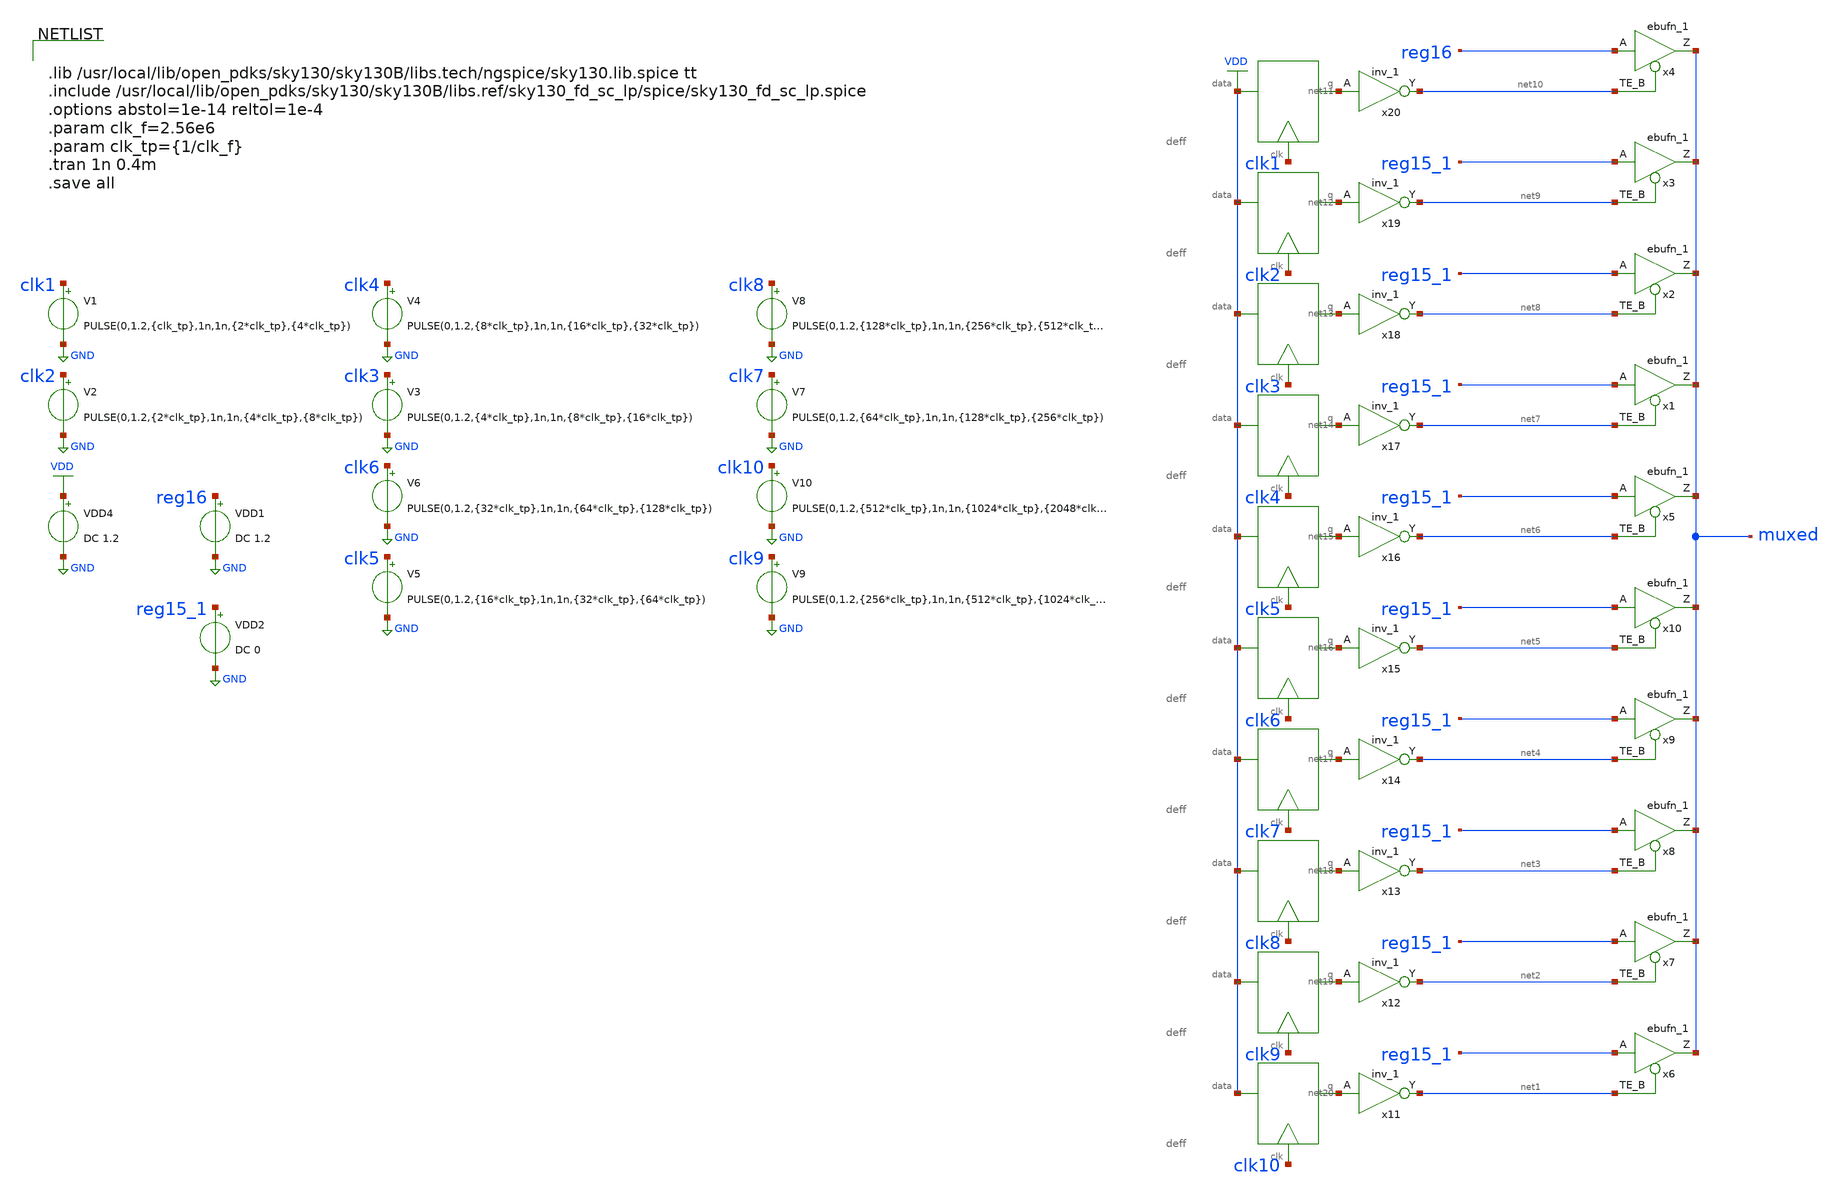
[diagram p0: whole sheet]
** sch_path: xschem/tryandtest/grayselection.sch
**.subckt grayselection
V1 clk1 GND PULSE(0,1.2,{clk_tp},1n,1n,{2*clk_tp},{4*clk_tp})
VDD4 VDD GND DC 1.2
V2 clk2 GND PULSE(0,1.2,{2*clk_tp},1n,1n,{4*clk_tp},{8*clk_tp})
V3 clk3 GND PULSE(0,1.2,{4*clk_tp},1n,1n,{8*clk_tp},{16*clk_tp})
V4 clk4 GND PULSE(0,1.2,{8*clk_tp},1n,1n,{16*clk_tp},{32*clk_tp})
V5 clk5 GND PULSE(0,1.2,{16*clk_tp},1n,1n,{32*clk_tp},{64*clk_tp})
V6 clk6 GND PULSE(0,1.2,{32*clk_tp},1n,1n,{64*clk_tp},{128*clk_tp})
V7 clk7 GND PULSE(0,1.2,{64*clk_tp},1n,1n,{128*clk_tp},{256*clk_tp})
V8 clk8 GND PULSE(0,1.2,{128*clk_tp},1n,1n,{256*clk_tp},{512*clk_tp})
V9 clk9 GND PULSE(0,1.2,{256*clk_tp},1n,1n,{512*clk_tp},{1024*clk_tp})
V10 clk10 GND PULSE(0,1.2,{512*clk_tp},1n,1n,{1024*clk_tp},{2048*clk_tp})
VDD1 reg16 GND DC 1.2
VDD2 reg15_1 GND DC 0
X1 VDD clk1 net11 deff
X1 VDD clk2 net12 deff
X1 VDD clk3 net13 deff
X1 VDD clk4 net14 deff
X1 VDD clk5 net15 deff
x5 reg15_1 net6 GND GND VDD VDD muxed sky130_fd_sc_lp__ebufn_1
X1 VDD clk6 net16 deff
X1 VDD clk7 net17 deff
X1 VDD clk8 net18 deff
X1 VDD clk9 net19 deff
X1 VDD clk10 net20 deff
x11 net20 GND GND VDD VDD net1 sky130_fd_sc_lp__inv_1
x12 net19 GND GND VDD VDD net2 sky130_fd_sc_lp__inv_1
x13 net18 GND GND VDD VDD net3 sky130_fd_sc_lp__inv_1
x14 net17 GND GND VDD VDD net4 sky130_fd_sc_lp__inv_1
x15 net16 GND GND VDD VDD net5 sky130_fd_sc_lp__inv_1
x16 net15 GND GND VDD VDD net6 sky130_fd_sc_lp__inv_1
x17 net14 GND GND VDD VDD net7 sky130_fd_sc_lp__inv_1
x18 net13 GND GND VDD VDD net8 sky130_fd_sc_lp__inv_1
x19 net12 GND GND VDD VDD net9 sky130_fd_sc_lp__inv_1
x20 net11 GND GND VDD VDD net10 sky130_fd_sc_lp__inv_1
x1 reg15_1 net7 GND GND VDD VDD muxed sky130_fd_sc_lp__ebufn_1
x2 reg15_1 net8 GND GND VDD VDD muxed sky130_fd_sc_lp__ebufn_1
x3 reg15_1 net9 GND GND VDD VDD muxed sky130_fd_sc_lp__ebufn_1
x4 reg16 net10 GND GND VDD VDD muxed sky130_fd_sc_lp__ebufn_1
x6 reg15_1 net1 GND GND VDD VDD muxed sky130_fd_sc_lp__ebufn_1
x7 reg15_1 net2 GND GND VDD VDD muxed sky130_fd_sc_lp__ebufn_1
x8 reg15_1 net3 GND GND VDD VDD muxed sky130_fd_sc_lp__ebufn_1
x9 reg15_1 net4 GND GND VDD VDD muxed sky130_fd_sc_lp__ebufn_1
x10 reg15_1 net5 GND GND VDD VDD muxed sky130_fd_sc_lp__ebufn_1
**** begin user architecture code


.lib /usr/local/lib/open_pdks/sky130/sky130B/libs.tech/ngspice/sky130.lib.spice tt
.include /usr/local/lib/open_pdks/sky130/sky130B/libs.ref/sky130_fd_sc_lp/spice/sky130_fd_sc_lp.spice
.options abstol=1e-14 reltol=1e-4
.param clk_f=2.56e6
.param clk_tp={1/clk_f}
.tran 1n 0.4m
.save all


**** end user architecture code
**.ends

* expanding   symbol:  tryandtest/deff.sym # of pins=3
** sym_path: xschem/tryandtest/deff.sym
** sch_path: xschem/tryandtest/deff.sch
.subckt deff data clk q
*.ipin clk
*.ipin data
*.opin q
x3 net1 net2 clk GND GND VDD VDD q sky130_fd_sc_lp__mux2_1
x5 clk data rstb GND GND VDD VDD net1 sky130_fd_sc_lp__dfrtn_1
x1 clk data rstb GND GND VDD VDD net2 sky130_fd_sc_lp__dfrtp_1
.ends

.GLOBAL GND
.GLOBAL VDD
.end
